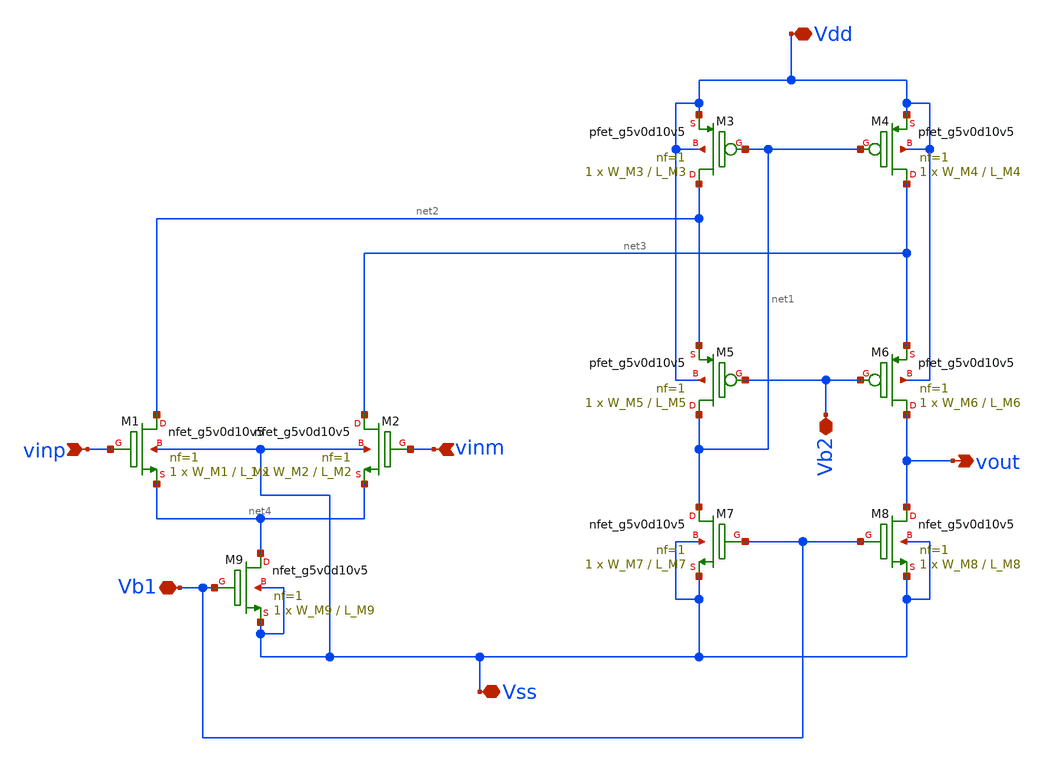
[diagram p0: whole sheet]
** sch_path: xschem/diff_pair_folded_cascode.sch
**.subckt diff_pair_folded_cascode Vdd vinm vinp Vb1 Vss Vb2 vout
*.iopin Vdd
*.ipin vinm
*.ipin vinp
*.iopin Vb1
*.iopin Vss
*.iopin Vb2
*.opin vout
XM1 net2 vinp net4 Vss sky130_fd_pr__nfet_g5v0d10v5 L=L_M1 W=W_M1 nf=1 ad='int((nf+1)/2) * W/nf * 0.29'
+ as='int((nf+2)/2) * W/nf * 0.29' pd='2*int((nf+1)/2) * (W/nf + 0.29)' ps='2*int((nf+2)/2) * (W/nf + 0.29)'
+ nrd='0.29 / W' nrs='0.29 / W' sa=0 sb=0 sd=0 mult=1 m=1
XM2 net3 vinm net4 Vss sky130_fd_pr__nfet_g5v0d10v5 L=L_M2 W=W_M2 nf=1 ad='int((nf+1)/2) * W/nf * 0.29'
+ as='int((nf+2)/2) * W/nf * 0.29' pd='2*int((nf+1)/2) * (W/nf + 0.29)' ps='2*int((nf+2)/2) * (W/nf + 0.29)'
+ nrd='0.29 / W' nrs='0.29 / W' sa=0 sb=0 sd=0 mult=1 m=1
XM4 net3 net1 Vdd Vdd sky130_fd_pr__pfet_g5v0d10v5 L=L_M4 W=W_M4 nf=1 ad='int((nf+1)/2) * W/nf * 0.29'
+ as='int((nf+2)/2) * W/nf * 0.29' pd='2*int((nf+1)/2) * (W/nf + 0.29)' ps='2*int((nf+2)/2) * (W/nf + 0.29)'
+ nrd='0.29 / W' nrs='0.29 / W' sa=0 sb=0 sd=0 mult=1 m=1
XM3 net2 net1 Vdd Vdd sky130_fd_pr__pfet_g5v0d10v5 L=L_M3 W=W_M3 nf=1 ad='int((nf+1)/2) * W/nf * 0.29'
+ as='int((nf+2)/2) * W/nf * 0.29' pd='2*int((nf+1)/2) * (W/nf + 0.29)' ps='2*int((nf+2)/2) * (W/nf + 0.29)'
+ nrd='0.29 / W' nrs='0.29 / W' sa=0 sb=0 sd=0 mult=1 m=1
XM9 net4 Vb1 Vss Vss sky130_fd_pr__nfet_g5v0d10v5 L=L_M9 W=W_M9 nf=1 ad='int((nf+1)/2) * W/nf * 0.29'
+ as='int((nf+2)/2) * W/nf * 0.29' pd='2*int((nf+1)/2) * (W/nf + 0.29)' ps='2*int((nf+2)/2) * (W/nf + 0.29)'
+ nrd='0.29 / W' nrs='0.29 / W' sa=0 sb=0 sd=0 mult=1 m=1
XM6 vout Vb2 net3 Vdd sky130_fd_pr__pfet_g5v0d10v5 L=L_M6 W=W_M6 nf=1 ad='int((nf+1)/2) * W/nf * 0.29'
+ as='int((nf+2)/2) * W/nf * 0.29' pd='2*int((nf+1)/2) * (W/nf + 0.29)' ps='2*int((nf+2)/2) * (W/nf + 0.29)'
+ nrd='0.29 / W' nrs='0.29 / W' sa=0 sb=0 sd=0 mult=1 m=1
XM5 net1 Vb2 net2 Vdd sky130_fd_pr__pfet_g5v0d10v5 L=L_M5 W=W_M5 nf=1 ad='int((nf+1)/2) * W/nf * 0.29'
+ as='int((nf+2)/2) * W/nf * 0.29' pd='2*int((nf+1)/2) * (W/nf + 0.29)' ps='2*int((nf+2)/2) * (W/nf + 0.29)'
+ nrd='0.29 / W' nrs='0.29 / W' sa=0 sb=0 sd=0 mult=1 m=1
XM7 net1 Vb1 Vss Vss sky130_fd_pr__nfet_g5v0d10v5 L=L_M7 W=W_M7 nf=1 ad='int((nf+1)/2) * W/nf * 0.29'
+ as='int((nf+2)/2) * W/nf * 0.29' pd='2*int((nf+1)/2) * (W/nf + 0.29)' ps='2*int((nf+2)/2) * (W/nf + 0.29)'
+ nrd='0.29 / W' nrs='0.29 / W' sa=0 sb=0 sd=0 mult=1 m=1
XM8 vout Vb1 Vss Vss sky130_fd_pr__nfet_g5v0d10v5 L=L_M8 W=W_M8 nf=1 ad='int((nf+1)/2) * W/nf * 0.29'
+ as='int((nf+2)/2) * W/nf * 0.29' pd='2*int((nf+1)/2) * (W/nf + 0.29)' ps='2*int((nf+2)/2) * (W/nf + 0.29)'
+ nrd='0.29 / W' nrs='0.29 / W' sa=0 sb=0 sd=0 mult=1 m=1
**.ends
.end
